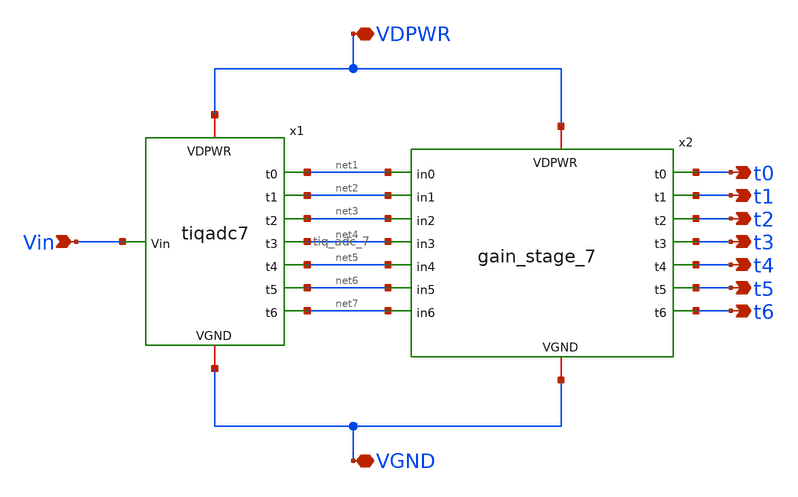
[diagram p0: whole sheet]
** sch_path: tt_um_emmersonv_tiq_adc/xschem/boosted_tiq_adc_7_xschem.sch
**.subckt boosted_tiq_adc_7_xschem VDPWR VGND Vin t0 t1 t2 t3 t4 t5 t6
*.iopin VDPWR
*.iopin VGND
*.ipin Vin
*.opin t0
*.opin t1
*.opin t2
*.opin t3
*.opin t4
*.opin t5
*.opin t6
x1 Vin VGND VDPWR net1 net2 net3 net4 net5 net6 net7 tiq_adc_7
x2 VDPWR VGND t0 net1 t1 net2 net3 t2 t3 net4 t4 net5 t5 net6 t6 net7 gain_stage_7
**.ends
.end
